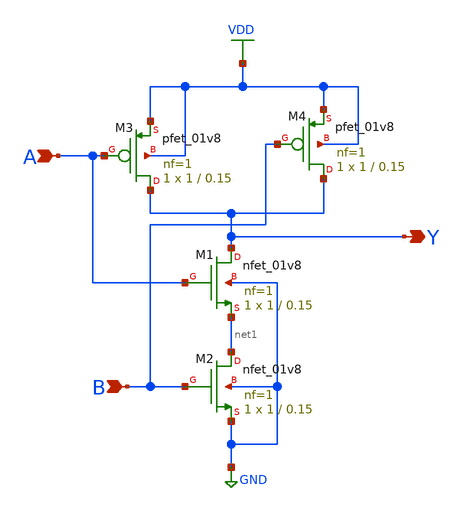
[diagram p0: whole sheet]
** sch_path: gates/NAND2_Gate.sch
**.subckt NAND2_Gate A B Y
*.ipin A
*.ipin B
*.opin Y
XM1 Y A net1 GND sky130_fd_pr__nfet_01v8 L=0.15 W=1 nf=1 ad='int((nf+1)/2) * W/nf * 0.29' as='int((nf+2)/2) * W/nf * 0.29'
+ pd='2*int((nf+1)/2) * (W/nf + 0.29)' ps='2*int((nf+2)/2) * (W/nf + 0.29)' nrd='0.29 / W' nrs='0.29 / W'
+ sa=0 sb=0 sd=0 mult=1 m=1
XM2 net1 B GND GND sky130_fd_pr__nfet_01v8 L=0.15 W=1 nf=1 ad='int((nf+1)/2) * W/nf * 0.29' as='int((nf+2)/2) * W/nf * 0.29'
+ pd='2*int((nf+1)/2) * (W/nf + 0.29)' ps='2*int((nf+2)/2) * (W/nf + 0.29)' nrd='0.29 / W' nrs='0.29 / W'
+ sa=0 sb=0 sd=0 mult=1 m=1
XM3 Y A VDD VDD sky130_fd_pr__pfet_01v8 L=0.15 W=1 nf=1 ad='int((nf+1)/2) * W/nf * 0.29' as='int((nf+2)/2) * W/nf * 0.29'
+ pd='2*int((nf+1)/2) * (W/nf + 0.29)' ps='2*int((nf+2)/2) * (W/nf + 0.29)' nrd='0.29 / W' nrs='0.29 / W'
+ sa=0 sb=0 sd=0 mult=1 m=1
XM4 Y B VDD VDD sky130_fd_pr__pfet_01v8 L=0.15 W=1 nf=1 ad='int((nf+1)/2) * W/nf * 0.29' as='int((nf+2)/2) * W/nf * 0.29'
+ pd='2*int((nf+1)/2) * (W/nf + 0.29)' ps='2*int((nf+2)/2) * (W/nf + 0.29)' nrd='0.29 / W' nrs='0.29 / W'
+ sa=0 sb=0 sd=0 mult=1 m=1
**.ends
.GLOBAL VDD
.GLOBAL GND
.end
